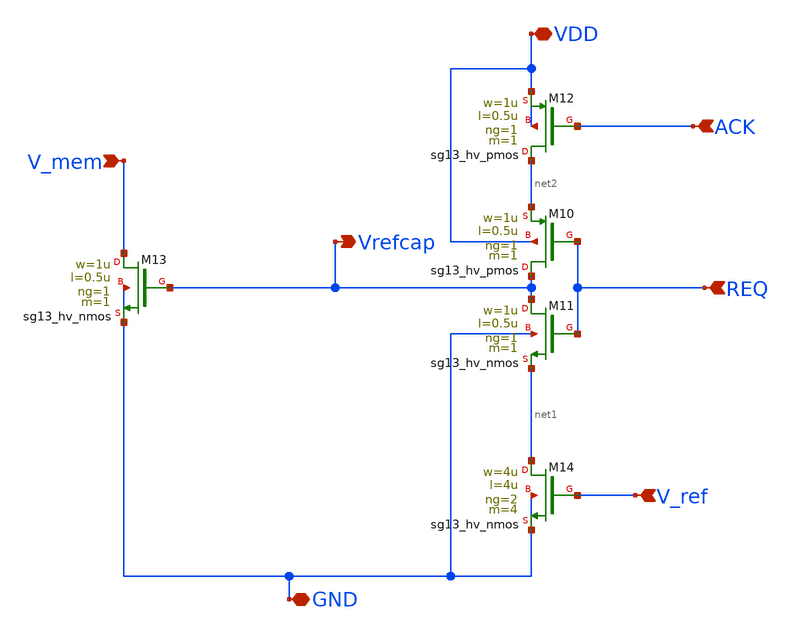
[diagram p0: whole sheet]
** sch_path: xschem/REF_system.sch
**.subckt REF_system VDD GND V_ref REQ ACK V_mem Vrefcap
*.iopin VDD
*.iopin GND
*.ipin V_ref
*.ipin REQ
*.ipin ACK
*.ipin V_mem
*.opin Vrefcap
XM10 Vrefcap REQ net2 VDD sg13_hv_pmos w=1u l=0.5u ng=1 m=1 mm_ok=1
XM11 Vrefcap REQ net1 GND sg13_hv_nmos w=1u l=0.5u ng=1 m=1 mm_ok=1
XM12 net2 ACK VDD VDD sg13_hv_pmos w=1u l=0.5u ng=1 m=1 mm_ok=1
XM13 V_mem Vrefcap GND GND sg13_hv_nmos w=1u l=0.5u ng=1 m=1 mm_ok=1
XM14 net1 V_ref GND GND sg13_hv_nmos w=4u l=4u ng=2 m=4 mm_ok=1
**.ends
.end
